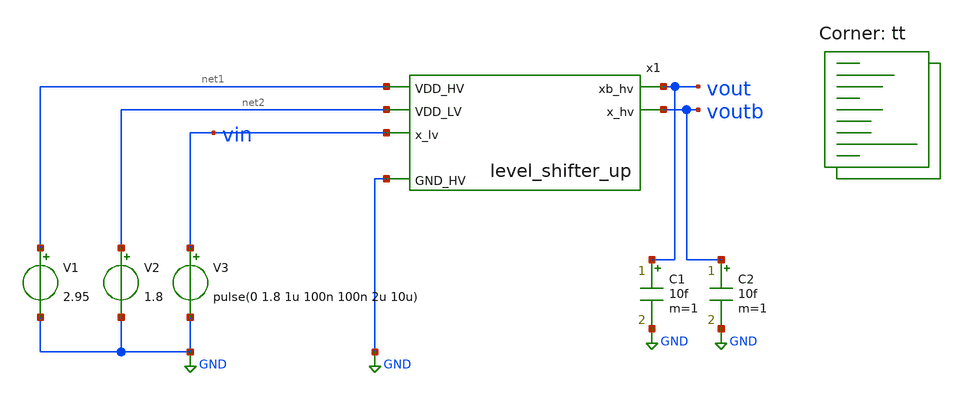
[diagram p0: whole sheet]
** sch_path: xschem/untitled.sch
**.subckt untitled
V1 net1 GND 2.95
V2 net2 GND 1.8
x1 net1 vout voutb vin GND net2 level_shifter_up
V3 vin GND pulse(0 1.8 1u 100n 100n 2u 10u)
C1 vout GND 10f m=1
C2 voutb GND 10f m=1
**** begin user architecture code


.tran 10n 5u
.save all
.control
foreach temp_val -40 25 85
   set temp=$temp_val
   foreach val 2.95 3.3 4.5 5.5
      alter v1 $val
      run
   end
end
*plot dc1.v(vout) dc2.v(vout) dc3.v(vout) dc4.v(vout) dc5.v(vout) dc6.v(vout) dc7.v(vout)
*+ dc8.v(vout) dc9.v(vout) dc10.v(vout) dc11.v(vout) dc12.v(vout)
plot tran1.v(vin) tran1.v(vout) tran2.v(vout) tran3.v(vout) tran4.v(vout) tran5.v(vout)
+ tran6.v(vout) tran7.v(vout) tran8.v(vout) tran9.v(vout)
.endc


.lib $::SKYWATER_MODELS/sky130.lib.spice tt
**** end user architecture code
**.ends

* expanding   symbol:  level_shifter_up.sym # of pins=6
** sym_path: xschem/level_shifter_up.sym
** sch_path: xschem/level_shifter_up.sch
.subckt level_shifter_up VDD_HV xb_hv x_hv x_lv GND_HV VDD_LV
*.ipin VDD_HV
*.ipin GND_HV
*.ipin x_lv
*.opin x_hv
*.opin xb_hv
*.ipin VDD_LV
XM65 xb_hv x_lv GND_HV GND_HV sky130_fd_pr__nfet_g5v0d10v5 L=0.5 W=1 nf=1 ad='int((nf+1)/2) * W/nf * 0.29'
+ as='int((nf+2)/2) * W/nf * 0.29' pd='2*int((nf+1)/2) * (W/nf + 0.29)' ps='2*int((nf+2)/2) * (W/nf + 0.29)'
+ nrd='0.29 / W' nrs='0.29 / W' sa=0 sb=0 sd=0 mult=1 m=1
XM66 x_hv xb_lv GND_HV GND_HV sky130_fd_pr__nfet_g5v0d10v5 L=0.5 W=1 nf=1 ad='int((nf+1)/2) * W/nf * 0.29'
+ as='int((nf+2)/2) * W/nf * 0.29' pd='2*int((nf+1)/2) * (W/nf + 0.29)' ps='2*int((nf+2)/2) * (W/nf + 0.29)'
+ nrd='0.29 / W' nrs='0.29 / W' sa=0 sb=0 sd=0 mult=1 m=1
XM67 xb_hv x_hv VDD_HV VDD_HV sky130_fd_pr__pfet_g5v0d10v5 L=0.5 W=0.5 nf=1 ad='int((nf+1)/2) * W/nf * 0.29'
+ as='int((nf+2)/2) * W/nf * 0.29' pd='2*int((nf+1)/2) * (W/nf + 0.29)' ps='2*int((nf+2)/2) * (W/nf + 0.29)'
+ nrd='0.29 / W' nrs='0.29 / W' sa=0 sb=0 sd=0 mult=1 m=1
XM68 x_hv xb_hv VDD_HV VDD_HV sky130_fd_pr__pfet_g5v0d10v5 L=0.5 W=0.5 nf=1 ad='int((nf+1)/2) * W/nf * 0.29'
+ as='int((nf+2)/2) * W/nf * 0.29' pd='2*int((nf+1)/2) * (W/nf + 0.29)' ps='2*int((nf+2)/2) * (W/nf + 0.29)'
+ nrd='0.29 / W' nrs='0.29 / W' sa=0 sb=0 sd=0 mult=1 m=1
XM1 xb_lv x_lv GND_HV GND_HV sky130_fd_pr__nfet_g5v0d10v5 L=0.5 W=1 nf=1 ad='int((nf+1)/2) * W/nf * 0.29'
+ as='int((nf+2)/2) * W/nf * 0.29' pd='2*int((nf+1)/2) * (W/nf + 0.29)' ps='2*int((nf+2)/2) * (W/nf + 0.29)'
+ nrd='0.29 / W' nrs='0.29 / W' sa=0 sb=0 sd=0 mult=1 m=1
XM3 xb_lv x_lv VDD_LV VDD_LV sky130_fd_pr__pfet_g5v0d10v5 L=0.5 W=2 nf=1 ad='int((nf+1)/2) * W/nf * 0.29'
+ as='int((nf+2)/2) * W/nf * 0.29' pd='2*int((nf+1)/2) * (W/nf + 0.29)' ps='2*int((nf+2)/2) * (W/nf + 0.29)'
+ nrd='0.29 / W' nrs='0.29 / W' sa=0 sb=0 sd=0 mult=1 m=1
.ends

.GLOBAL GND
.end
